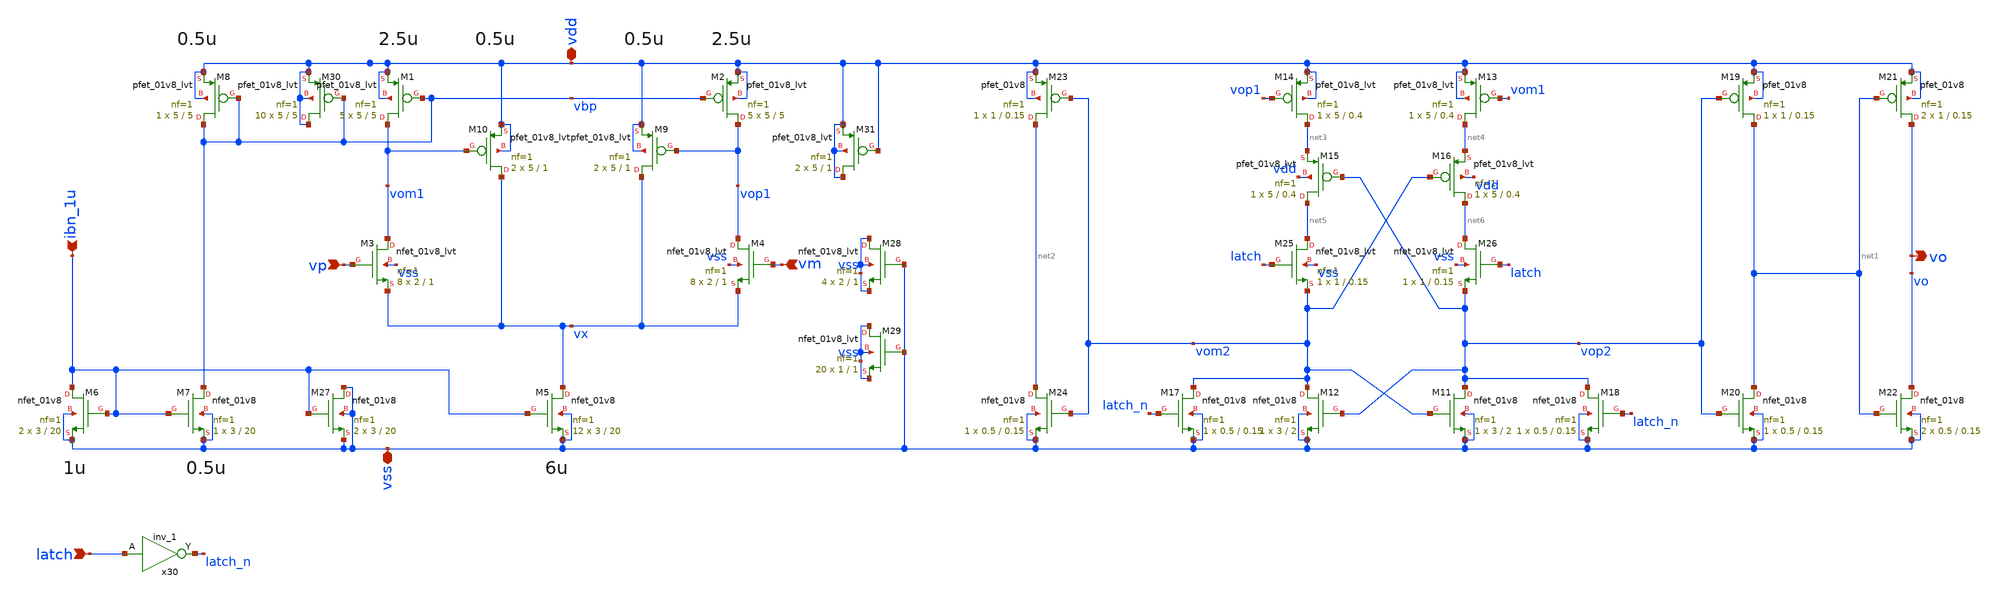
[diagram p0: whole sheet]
** sch_path: test/design/adc_comp.sch
**.subckt adc_comp vss vdd vp vm latch ibn_1u vo
*.iopin vss
*.iopin vdd
*.ipin vp
*.ipin vm
*.ipin latch
*.ipin ibn_1u
*.opin vo
XM3 vom1 vp vx vss sky130_fd_pr__nfet_01v8_lvt L=1 W=2 nf=1 ad='int((nf+1)/2) * W/nf * 0.29' as='int((nf+2)/2) * W/nf * 0.29'
+ pd='2*int((nf+1)/2) * (W/nf + 0.29)' ps='2*int((nf+2)/2) * (W/nf + 0.29)' nrd='0.29 / W' nrs='0.29 / W'
+ sa=0 sb=0 sd=0 mult=8 m=8
XM4 vop1 vm vx vss sky130_fd_pr__nfet_01v8_lvt L=1 W=2 nf=1 ad='int((nf+1)/2) * W/nf * 0.29' as='int((nf+2)/2) * W/nf * 0.29'
+ pd='2*int((nf+1)/2) * (W/nf + 0.29)' ps='2*int((nf+2)/2) * (W/nf + 0.29)' nrd='0.29 / W' nrs='0.29 / W'
+ sa=0 sb=0 sd=0 mult=8 m=8
XM2 vop1 vbp vdd vdd sky130_fd_pr__pfet_01v8_lvt L=5 W=5 nf=1 ad='int((nf+1)/2) * W/nf * 0.29' as='int((nf+2)/2) * W/nf * 0.29'
+ pd='2*int((nf+1)/2) * (W/nf + 0.29)' ps='2*int((nf+2)/2) * (W/nf + 0.29)' nrd='0.29 / W' nrs='0.29 / W'
+ sa=0 sb=0 sd=0 mult=5 m=5
XM1 vom1 vbp vdd vdd sky130_fd_pr__pfet_01v8_lvt L=5 W=5 nf=1 ad='int((nf+1)/2) * W/nf * 0.29' as='int((nf+2)/2) * W/nf * 0.29'
+ pd='2*int((nf+1)/2) * (W/nf + 0.29)' ps='2*int((nf+2)/2) * (W/nf + 0.29)' nrd='0.29 / W' nrs='0.29 / W'
+ sa=0 sb=0 sd=0 mult=5 m=5
XM6 ibn_1u ibn_1u vss vss sky130_fd_pr__nfet_01v8 L=20 W=3 nf=1 ad='int((nf+1)/2) * W/nf * 0.29' as='int((nf+2)/2) * W/nf * 0.29'
+ pd='2*int((nf+1)/2) * (W/nf + 0.29)' ps='2*int((nf+2)/2) * (W/nf + 0.29)' nrd='0.29 / W' nrs='0.29 / W'
+ sa=0 sb=0 sd=0 mult=2 m=2
XM5 vx ibn_1u vss vss sky130_fd_pr__nfet_01v8 L=20 W=3 nf=1 ad='int((nf+1)/2) * W/nf * 0.29' as='int((nf+2)/2) * W/nf * 0.29'
+ pd='2*int((nf+1)/2) * (W/nf + 0.29)' ps='2*int((nf+2)/2) * (W/nf + 0.29)' nrd='0.29 / W' nrs='0.29 / W'
+ sa=0 sb=0 sd=0 mult=12 m=12
XM7 vbp ibn_1u vss vss sky130_fd_pr__nfet_01v8 L=20 W=3 nf=1 ad='int((nf+1)/2) * W/nf * 0.29' as='int((nf+2)/2) * W/nf * 0.29'
+ pd='2*int((nf+1)/2) * (W/nf + 0.29)' ps='2*int((nf+2)/2) * (W/nf + 0.29)' nrd='0.29 / W' nrs='0.29 / W'
+ sa=0 sb=0 sd=0 mult=1 m=1
XM8 vbp vbp vdd vdd sky130_fd_pr__pfet_01v8_lvt L=5 W=5 nf=1 ad='int((nf+1)/2) * W/nf * 0.29' as='int((nf+2)/2) * W/nf * 0.29'
+ pd='2*int((nf+1)/2) * (W/nf + 0.29)' ps='2*int((nf+2)/2) * (W/nf + 0.29)' nrd='0.29 / W' nrs='0.29 / W'
+ sa=0 sb=0 sd=0 mult=1 m=1
XM9 vx vop1 vdd vdd sky130_fd_pr__pfet_01v8_lvt L=1 W=5 nf=1 ad='int((nf+1)/2) * W/nf * 0.29' as='int((nf+2)/2) * W/nf * 0.29'
+ pd='2*int((nf+1)/2) * (W/nf + 0.29)' ps='2*int((nf+2)/2) * (W/nf + 0.29)' nrd='0.29 / W' nrs='0.29 / W'
+ sa=0 sb=0 sd=0 mult=2 m=2
XM10 vx vom1 vdd vdd sky130_fd_pr__pfet_01v8_lvt L=1 W=5 nf=1 ad='int((nf+1)/2) * W/nf * 0.29' as='int((nf+2)/2) * W/nf * 0.29'
+ pd='2*int((nf+1)/2) * (W/nf + 0.29)' ps='2*int((nf+2)/2) * (W/nf + 0.29)' nrd='0.29 / W' nrs='0.29 / W'
+ sa=0 sb=0 sd=0 mult=2 m=2
XM11 vop2 vom2 vss vss sky130_fd_pr__nfet_01v8 L=2 W=3 nf=1 ad='int((nf+1)/2) * W/nf * 0.29' as='int((nf+2)/2) * W/nf * 0.29'
+ pd='2*int((nf+1)/2) * (W/nf + 0.29)' ps='2*int((nf+2)/2) * (W/nf + 0.29)' nrd='0.29 / W' nrs='0.29 / W'
+ sa=0 sb=0 sd=0 mult=1 m=1
XM12 vom2 vop2 vss vss sky130_fd_pr__nfet_01v8 L=2 W=3 nf=1 ad='int((nf+1)/2) * W/nf * 0.29' as='int((nf+2)/2) * W/nf * 0.29'
+ pd='2*int((nf+1)/2) * (W/nf + 0.29)' ps='2*int((nf+2)/2) * (W/nf + 0.29)' nrd='0.29 / W' nrs='0.29 / W'
+ sa=0 sb=0 sd=0 mult=1 m=1
XM13 net4 vom1 vdd vdd sky130_fd_pr__pfet_01v8_lvt L=0.4 W=5 nf=1 ad='int((nf+1)/2) * W/nf * 0.29' as='int((nf+2)/2) * W/nf * 0.29'
+ pd='2*int((nf+1)/2) * (W/nf + 0.29)' ps='2*int((nf+2)/2) * (W/nf + 0.29)' nrd='0.29 / W' nrs='0.29 / W'
+ sa=0 sb=0 sd=0 mult=1 m=1
XM14 net3 vop1 vdd vdd sky130_fd_pr__pfet_01v8_lvt L=0.4 W=5 nf=1 ad='int((nf+1)/2) * W/nf * 0.29' as='int((nf+2)/2) * W/nf * 0.29'
+ pd='2*int((nf+1)/2) * (W/nf + 0.29)' ps='2*int((nf+2)/2) * (W/nf + 0.29)' nrd='0.29 / W' nrs='0.29 / W'
+ sa=0 sb=0 sd=0 mult=1 m=1
XM17 vom2 latch_n vss vss sky130_fd_pr__nfet_01v8 L=0.15 W=0.5 nf=1 ad='int((nf+1)/2) * W/nf * 0.29'
+ as='int((nf+2)/2) * W/nf * 0.29' pd='2*int((nf+1)/2) * (W/nf + 0.29)' ps='2*int((nf+2)/2) * (W/nf + 0.29)'
+ nrd='0.29 / W' nrs='0.29 / W' sa=0 sb=0 sd=0 mult=1 m=1
XM18 vop2 latch_n vss vss sky130_fd_pr__nfet_01v8 L=0.15 W=0.5 nf=1 ad='int((nf+1)/2) * W/nf * 0.29'
+ as='int((nf+2)/2) * W/nf * 0.29' pd='2*int((nf+1)/2) * (W/nf + 0.29)' ps='2*int((nf+2)/2) * (W/nf + 0.29)'
+ nrd='0.29 / W' nrs='0.29 / W' sa=0 sb=0 sd=0 mult=1 m=1
XM19 net1 vop2 vdd vdd sky130_fd_pr__pfet_01v8 L=0.15 W=1 nf=1 ad='int((nf+1)/2) * W/nf * 0.29' as='int((nf+2)/2) * W/nf * 0.29'
+ pd='2*int((nf+1)/2) * (W/nf + 0.29)' ps='2*int((nf+2)/2) * (W/nf + 0.29)' nrd='0.29 / W' nrs='0.29 / W'
+ sa=0 sb=0 sd=0 mult=1 m=1
XM20 net1 vop2 vss vss sky130_fd_pr__nfet_01v8 L=0.15 W=0.5 nf=1 ad='int((nf+1)/2) * W/nf * 0.29' as='int((nf+2)/2) * W/nf * 0.29'
+ pd='2*int((nf+1)/2) * (W/nf + 0.29)' ps='2*int((nf+2)/2) * (W/nf + 0.29)' nrd='0.29 / W' nrs='0.29 / W'
+ sa=0 sb=0 sd=0 mult=1 m=1
XM21 vo net1 vdd vdd sky130_fd_pr__pfet_01v8 L=0.15 W=1 nf=1 ad='int((nf+1)/2) * W/nf * 0.29' as='int((nf+2)/2) * W/nf * 0.29'
+ pd='2*int((nf+1)/2) * (W/nf + 0.29)' ps='2*int((nf+2)/2) * (W/nf + 0.29)' nrd='0.29 / W' nrs='0.29 / W'
+ sa=0 sb=0 sd=0 mult=2 m=2
XM22 vo net1 vss vss sky130_fd_pr__nfet_01v8 L=0.15 W=0.5 nf=1 ad='int((nf+1)/2) * W/nf * 0.29' as='int((nf+2)/2) * W/nf * 0.29'
+ pd='2*int((nf+1)/2) * (W/nf + 0.29)' ps='2*int((nf+2)/2) * (W/nf + 0.29)' nrd='0.29 / W' nrs='0.29 / W'
+ sa=0 sb=0 sd=0 mult=2 m=2
XM23 net2 vom2 vdd vdd sky130_fd_pr__pfet_01v8 L=0.15 W=1 nf=1 ad='int((nf+1)/2) * W/nf * 0.29' as='int((nf+2)/2) * W/nf * 0.29'
+ pd='2*int((nf+1)/2) * (W/nf + 0.29)' ps='2*int((nf+2)/2) * (W/nf + 0.29)' nrd='0.29 / W' nrs='0.29 / W'
+ sa=0 sb=0 sd=0 mult=1 m=1
XM24 net2 vom2 vss vss sky130_fd_pr__nfet_01v8 L=0.15 W=0.5 nf=1 ad='int((nf+1)/2) * W/nf * 0.29' as='int((nf+2)/2) * W/nf * 0.29'
+ pd='2*int((nf+1)/2) * (W/nf + 0.29)' ps='2*int((nf+2)/2) * (W/nf + 0.29)' nrd='0.29 / W' nrs='0.29 / W'
+ sa=0 sb=0 sd=0 mult=1 m=1
XM15 net5 vop2 net3 vdd sky130_fd_pr__pfet_01v8_lvt L=0.4 W=5 nf=1 ad='int((nf+1)/2) * W/nf * 0.29' as='int((nf+2)/2) * W/nf * 0.29'
+ pd='2*int((nf+1)/2) * (W/nf + 0.29)' ps='2*int((nf+2)/2) * (W/nf + 0.29)' nrd='0.29 / W' nrs='0.29 / W'
+ sa=0 sb=0 sd=0 mult=1 m=1
XM16 net6 vom2 net4 vdd sky130_fd_pr__pfet_01v8_lvt L=0.4 W=5 nf=1 ad='int((nf+1)/2) * W/nf * 0.29' as='int((nf+2)/2) * W/nf * 0.29'
+ pd='2*int((nf+1)/2) * (W/nf + 0.29)' ps='2*int((nf+2)/2) * (W/nf + 0.29)' nrd='0.29 / W' nrs='0.29 / W'
+ sa=0 sb=0 sd=0 mult=1 m=1
XM25 net5 latch vom2 vss sky130_fd_pr__nfet_01v8_lvt L=0.15 W=1 nf=1 ad='int((nf+1)/2) * W/nf * 0.29'
+ as='int((nf+2)/2) * W/nf * 0.29' pd='2*int((nf+1)/2) * (W/nf + 0.29)' ps='2*int((nf+2)/2) * (W/nf + 0.29)'
+ nrd='0.29 / W' nrs='0.29 / W' sa=0 sb=0 sd=0 mult=1 m=1
XM26 net6 latch vop2 vss sky130_fd_pr__nfet_01v8_lvt L=0.15 W=1 nf=1 ad='int((nf+1)/2) * W/nf * 0.29'
+ as='int((nf+2)/2) * W/nf * 0.29' pd='2*int((nf+1)/2) * (W/nf + 0.29)' ps='2*int((nf+2)/2) * (W/nf + 0.29)'
+ nrd='0.29 / W' nrs='0.29 / W' sa=0 sb=0 sd=0 mult=1 m=1
x30 latch vss vss vdd vdd latch_n sky130_fd_sc_hd__inv_1
XM27 vss ibn_1u vss vss sky130_fd_pr__nfet_01v8 L=20 W=3 nf=1 ad='int((nf+1)/2) * W/nf * 0.29' as='int((nf+2)/2) * W/nf * 0.29'
+ pd='2*int((nf+1)/2) * (W/nf + 0.29)' ps='2*int((nf+2)/2) * (W/nf + 0.29)' nrd='0.29 / W' nrs='0.29 / W'
+ sa=0 sb=0 sd=0 mult=2 m=2
XM28 vss vss vss vss sky130_fd_pr__nfet_01v8_lvt L=1 W=2 nf=1 ad='int((nf+1)/2) * W/nf * 0.29' as='int((nf+2)/2) * W/nf * 0.29'
+ pd='2*int((nf+1)/2) * (W/nf + 0.29)' ps='2*int((nf+2)/2) * (W/nf + 0.29)' nrd='0.29 / W' nrs='0.29 / W'
+ sa=0 sb=0 sd=0 mult=4 m=4
XM29 vss vss vss vss sky130_fd_pr__nfet_01v8_lvt L=1 W=1 nf=1 ad='int((nf+1)/2) * W/nf * 0.29' as='int((nf+2)/2) * W/nf * 0.29'
+ pd='2*int((nf+1)/2) * (W/nf + 0.29)' ps='2*int((nf+2)/2) * (W/nf + 0.29)' nrd='0.29 / W' nrs='0.29 / W'
+ sa=0 sb=0 sd=0 mult=20 m=20
XM30 vdd vbp vdd vdd sky130_fd_pr__pfet_01v8_lvt L=5 W=5 nf=1 ad='int((nf+1)/2) * W/nf * 0.29' as='int((nf+2)/2) * W/nf * 0.29'
+ pd='2*int((nf+1)/2) * (W/nf + 0.29)' ps='2*int((nf+2)/2) * (W/nf + 0.29)' nrd='0.29 / W' nrs='0.29 / W'
+ sa=0 sb=0 sd=0 mult=10 m=10
XM31 vdd vdd vdd vdd sky130_fd_pr__pfet_01v8_lvt L=1 W=5 nf=1 ad='int((nf+1)/2) * W/nf * 0.29' as='int((nf+2)/2) * W/nf * 0.29'
+ pd='2*int((nf+1)/2) * (W/nf + 0.29)' ps='2*int((nf+2)/2) * (W/nf + 0.29)' nrd='0.29 / W' nrs='0.29 / W'
+ sa=0 sb=0 sd=0 mult=2 m=2
**.ends
.end
